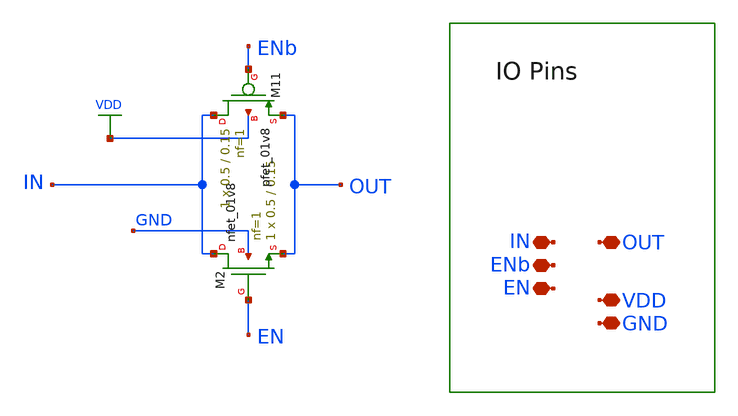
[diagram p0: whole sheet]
** sch_path: scope_sky130_v1/tgate.sch
**.subckt tgate IN VDD GND ENb EN OUT
*.iopin IN
*.iopin VDD
*.iopin GND
*.iopin ENb
*.iopin EN
*.iopin OUT
XM2 IN EN OUT GND sky130_fd_pr__nfet_01v8 L=0.15 W=0.5 nf=1 ad='int((1 + 1)/2) * 0.5 / 1 * 0.29' as='int((1 + 2)/2) * 0.5 / 1 * 0.29'
+ pd='2*int((1 + 1)/2) * (0.5 / 1 + 0.29)' ps='2*int((1 + 2)/2) * (0.5 / 1 + 0.29)' nrd='0.29 / 0.5 ' nrs='0.29 / 0.5 '
+ sa=0 sb=0 sd=0 mult=1 m=1
XM11 IN ENb OUT VDD sky130_fd_pr__pfet_01v8 L=0.15 W=0.5 nf=1 ad='int((nf+1)/2) * W/nf * 0.29' as='int((nf+2)/2) * W/nf * 0.29'
+ pd='2*int((nf+1)/2) * (W/nf + 0.29)' ps='2*int((nf+2)/2) * (W/nf + 0.29)' nrd='0.29 / W' nrs='0.29 / W'
+ sa=0 sb=0 sd=0 mult=1 m=1
**.ends
.GLOBAL VDD
.end
